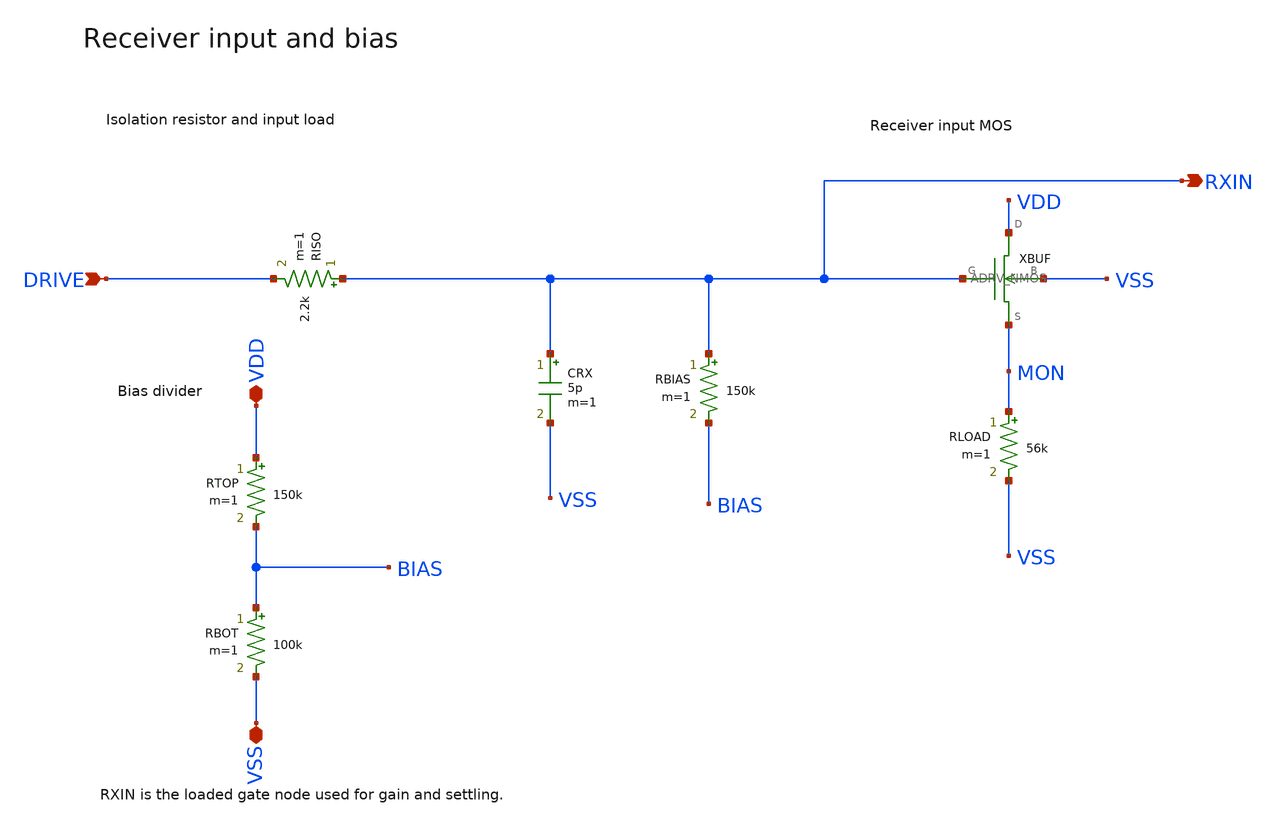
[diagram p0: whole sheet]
** sch_path: examples/sky130-programmable-gain/PGA_RECEIVER.sch
**.subckt PGA_RECEIVER DRIVE RXIN VDD VSS
*.ipin DRIVE
*.opin RXIN
*.iopin VDD
*.iopin VSS
RISO RXIN DRIVE 2.2k m=1
CRX RXIN VSS 5p m=1
RBIAS RXIN BIAS 150k m=1
XBUF VDD RXIN MON VSS sky130_fd_pr__nfet_01v8 w=4 l=0.5 nf=1 ad=1.2 as=1.2 pd=8.6 ps=8.6 m=1
RLOAD MON VSS 56k m=1
RTOP VDD BIAS 150k m=1
RBOT BIAS VSS 100k m=1
**.ends
.end
